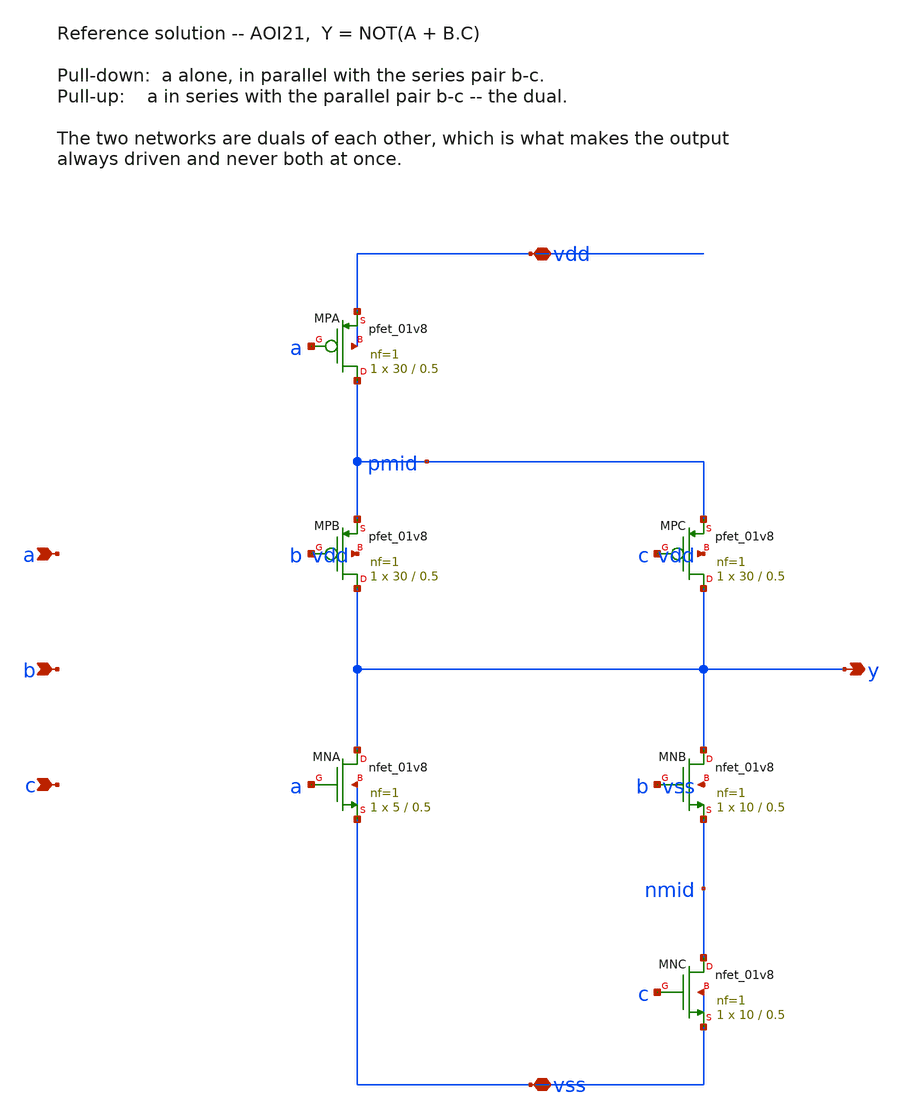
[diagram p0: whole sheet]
** sch_path: instructors/lab3/xschem/dut_aoi21.sch
**.subckt dut_aoi21 a b c y vdd vss
*.ipin a
*.ipin b
*.ipin c
*.opin y
*.iopin vdd
*.iopin vss
XMPA pmid a vdd vdd sky130_fd_pr__pfet_01v8 L=0.5 W=30 nf=1 ad='int((nf+1)/2) * W/nf * 0.29' as='int((nf+2)/2) * W/nf * 0.29'
+ pd='2*int((nf+1)/2) * (W/nf + 0.29)' ps='2*int((nf+2)/2) * (W/nf + 0.29)' nrd='0.29 / W' nrs='0.29 / W'
+ sa=0 sb=0 sd=0 mult=1 m=1
XMPB y b pmid vdd sky130_fd_pr__pfet_01v8 L=0.5 W=30 nf=1 ad='int((nf+1)/2) * W/nf * 0.29' as='int((nf+2)/2) * W/nf * 0.29'
+ pd='2*int((nf+1)/2) * (W/nf + 0.29)' ps='2*int((nf+2)/2) * (W/nf + 0.29)' nrd='0.29 / W' nrs='0.29 / W'
+ sa=0 sb=0 sd=0 mult=1 m=1
XMPC y c pmid vdd sky130_fd_pr__pfet_01v8 L=0.5 W=30 nf=1 ad='int((nf+1)/2) * W/nf * 0.29' as='int((nf+2)/2) * W/nf * 0.29'
+ pd='2*int((nf+1)/2) * (W/nf + 0.29)' ps='2*int((nf+2)/2) * (W/nf + 0.29)' nrd='0.29 / W' nrs='0.29 / W'
+ sa=0 sb=0 sd=0 mult=1 m=1
XMNA y a vss vss sky130_fd_pr__nfet_01v8 L=0.5 W=5 nf=1 ad='int((1 + 1)/2) * 5 / 1 * 0.29' as='int((1 + 2)/2) * 5 / 1 * 0.29'
+ pd='2*int((1 + 1)/2) * (5 / 1 + 0.29)' ps='2*int((1 + 2)/2) * (5 / 1 + 0.29)' nrd='0.29 / 5 ' nrs='0.29 / 5 '
+ sa=0 sb=0 sd=0 mult=1 m=1
XMNB y b nmid vss sky130_fd_pr__nfet_01v8 L=0.5 W=10 nf=1 ad='int((1 + 1)/2) * 10 / 1 * 0.29' as='int((1 + 2)/2) * 10 / 1 * 0.29'
+ pd='2*int((1 + 1)/2) * (10 / 1 + 0.29)' ps='2*int((1 + 2)/2) * (10 / 1 + 0.29)' nrd='0.29 / 10 ' nrs='0.29 / 10 '
+ sa=0 sb=0 sd=0 mult=1 m=1
XMNC nmid c vss vss sky130_fd_pr__nfet_01v8 L=0.5 W=10 nf=1 ad='int((1 + 1)/2) * 10 / 1 * 0.29' as='int((1 + 2)/2) * 10 / 1 * 0.29'
+ pd='2*int((1 + 1)/2) * (10 / 1 + 0.29)' ps='2*int((1 + 2)/2) * (10 / 1 + 0.29)' nrd='0.29 / 10 ' nrs='0.29 / 10 '
+ sa=0 sb=0 sd=0 mult=1 m=1
**.ends
.end
